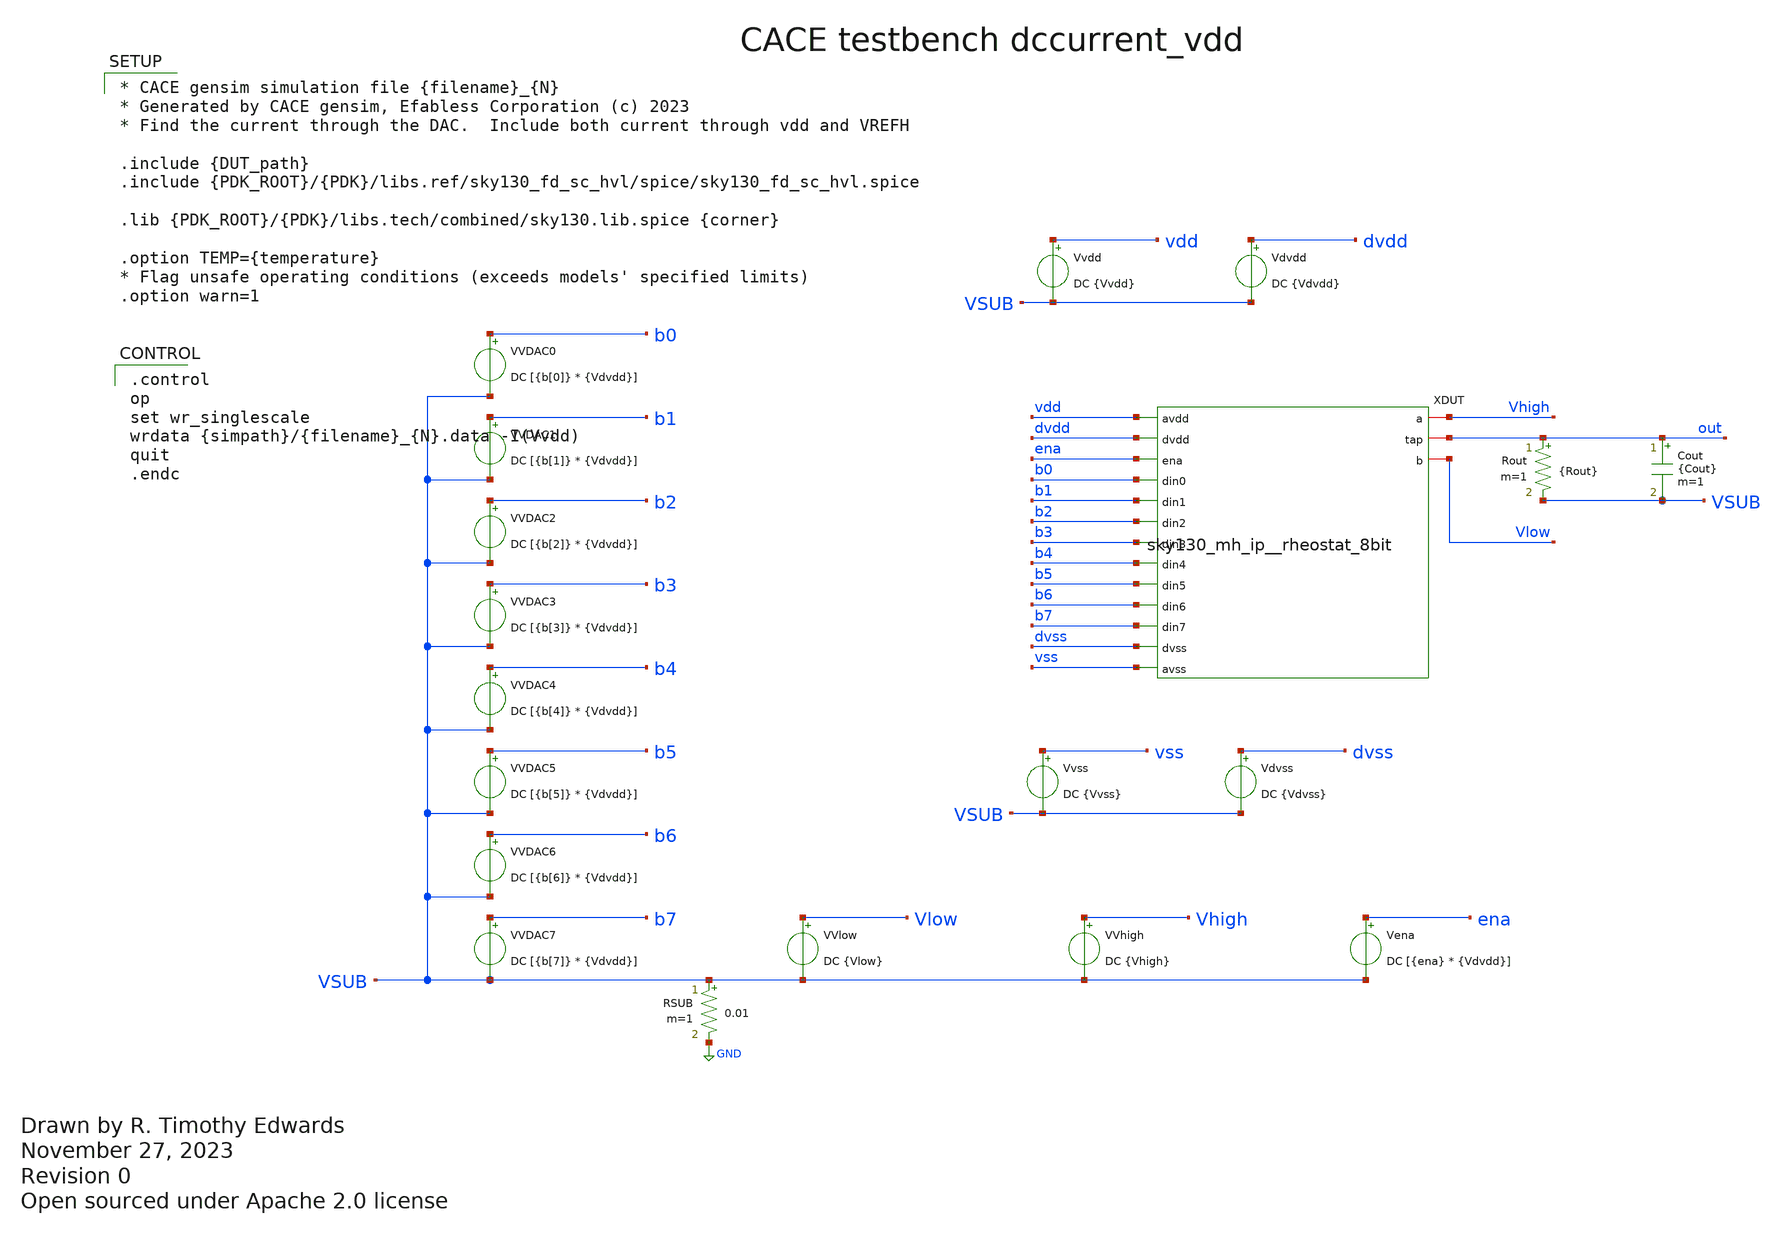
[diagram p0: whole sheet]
** sch_path: cace/dccurrent_vdd.sch
* Open sourced under Apache 2.0 license
**.subckt dccurrent_vdd
VVDAC7 b7 VSUB DC [{b[7]} * {Vdvdd}]
VVDAC1 b1 VSUB DC [{b[1]} * {Vdvdd}]
VVDAC2 b2 VSUB DC [{b[2]} * {Vdvdd}]
VVDAC3 b3 VSUB DC [{b[3]} * {Vdvdd}]
VVDAC4 b4 VSUB DC [{b[4]} * {Vdvdd}]
VVDAC5 b5 VSUB DC [{b[5]} * {Vdvdd}]
VVDAC6 b6 VSUB DC [{b[6]} * {Vdvdd}]
VVDAC0 b0 VSUB DC [{b[0]} * {Vdvdd}]
VVlow Vlow VSUB DC {Vlow}
VVhigh Vhigh VSUB DC {Vhigh}
Vena ena VSUB DC [{ena} * {Vdvdd}]
Vvss vss VSUB DC {Vvss}
Rout out VSUB {Rout} m=1
Cout out VSUB {Cout} m=1
Vdvss dvss VSUB DC {Vdvss}
Vvdd vdd VSUB DC {Vvdd}
Vdvdd dvdd VSUB DC {Vdvdd}
RSUB VSUB GND 0.01 m=1
XDUT vdd dvdd ena b0 Vhigh b1 b2 out b3 Vlow b4 b5 b6 b7 dvss vss sky130_mh_ip__rheostat_8bit
**** begin user architecture code

.control
op
set wr_singlescale
wrdata {simpath}/{filename}_{N}.data -I(Vvdd)
quit
.endc



* CACE gensim simulation file {filename}_{N}
* Generated by CACE gensim, Efabless Corporation (c) 2023
* Find the current through the DAC.  Include both current through vdd and VREFH

.include {DUT_path}
.include {PDK_ROOT}/{PDK}/libs.ref/sky130_fd_sc_hvl/spice/sky130_fd_sc_hvl.spice

.lib {PDK_ROOT}/{PDK}/libs.tech/combined/sky130.lib.spice {corner}

.option TEMP={temperature}
* Flag unsafe operating conditions (exceeds models' specified limits)
.option warn=1


**** end user architecture code
**.ends

* expanding   symbol:  sky130_mh_ip__rheostat_8bit.sym # of pins=16
** sym_path: xschem/sky130_mh_ip__rheostat_8bit.sym
** sch_path: xschem/sky130_mh_ip__rheostat_8bit.sch
.subckt sky130_mh_ip__rheostat_8bit avdd dvdd ena din0 a din1 din2 tap din3 b din4 din5 din6 din7 dvss avss
*.ipin din0
*.ipin din1
*.ipin din2
*.ipin din3
*.ipin din4
*.ipin din5
*.ipin din6
*.ipin din7
*.iopin a
*.iopin tap
*.iopin b
*.ipin dvss
*.ipin avdd
*.ipin avss
*.ipin ena
*.ipin dvdd
x1 avdd nb0 nb5 nb6 nb3 nb4 nb1 nb7 nb2 a tap pb3 pb2 pb4 pb1 pb5 pb7 pb6 pb0 avss 8bit_half_rheostat
x2 avdd dvdd nb0 ena pb0 din0 dvss avss double_output_buffer
x3 avdd dvdd nb1 ena pb1 din1 dvss avss double_output_buffer
x4 avdd dvdd nb2 ena pb2 din2 dvss avss double_output_buffer
x5 avdd dvdd nb3 ena pb3 din3 dvss avss double_output_buffer
x6 avdd dvdd nb4 ena pb4 din4 dvss avss double_output_buffer
x7 avdd dvdd nb5 ena pb5 din5 dvss avss double_output_buffer
x8 avdd dvdd nb6 ena pb6 din6 dvss avss double_output_buffer
x9 avdd dvdd nb7 ena pb7 din7 dvss avss double_output_buffer
x10 avdd pb0 pb5 pb6 pb3 pb4 pb1 pb7 pb2 tap b nb3 nb2 nb4 nb1 nb5 nb7 nb6 nb0 avss 8bit_half_rheostat
.ends


* expanding   symbol:  8bit_half_rheostat.sym # of pins=20
** sym_path: xschem/8bit_half_rheostat.sym
** sch_path: xschem/8bit_half_rheostat.sch
.subckt 8bit_half_rheostat avdd inn0 inn5 inn6 inn3 inn4 inn1 inn7 inn2 a b inp3 inp2 inp4 inp1 inp5 inp7 inp6 inp0 avss
*.iopin b
*.iopin a
*.ipin inn0
*.ipin inn1
*.ipin inn2
*.ipin inn3
*.ipin inn4
*.ipin inn5
*.ipin inn6
*.ipin inn7
*.ipin inp0
*.ipin inp1
*.ipin inp2
*.ipin inp3
*.ipin inp4
*.ipin inp5
*.ipin inp6
*.ipin inp7
*.ipin avdd
*.ipin avss
XM17 a inn0 net1 avdd sky130_fd_pr__pfet_g5v0d10v5 L=0.5 W=10 nf=1 ad='int((nf+1)/2) * W/nf * 0.29' as='int((nf+2)/2)
+ * W/nf * 0.29' pd='2*int((nf+1)/2) * (W/nf + 0.29)' ps='2*int((nf+2)/2) * (W/nf + 0.29)' nrd='0.29 /
+ W' nrs='0.29 / W' sa=0 sb=0 sd=0 mult=1 m=1
XM18 a inp0 net1 avss sky130_fd_pr__nfet_g5v0d10v5 L=0.5 W=10 nf=1 ad='int((nf+1)/2) * W/nf * 0.29' as='int((nf+2)/2)
+ * W/nf * 0.29' pd='2*int((nf+1)/2) * (W/nf + 0.29)' ps='2*int((nf+2)/2) * (W/nf + 0.29)' nrd='0.29 /
+ W' nrs='0.29 / W' sa=0 sb=0 sd=0 mult=1 m=1
XM19 net1 inn1 net2 avdd sky130_fd_pr__pfet_g5v0d10v5 L=0.5 W=10 nf=1 ad='int((nf+1)/2) * W/nf * 0.29' as='int((nf+2)/2)
+ * W/nf * 0.29' pd='2*int((nf+1)/2) * (W/nf + 0.29)' ps='2*int((nf+2)/2) * (W/nf + 0.29)' nrd='0.29 /
+ W' nrs='0.29 / W' sa=0 sb=0 sd=0 mult=1 m=1
XM20 net1 inp1 net2 avss sky130_fd_pr__nfet_g5v0d10v5 L=0.5 W=10 nf=1 ad='int((nf+1)/2) * W/nf * 0.29' as='int((nf+2)/2)
+ * W/nf * 0.29' pd='2*int((nf+1)/2) * (W/nf + 0.29)' ps='2*int((nf+2)/2) * (W/nf + 0.29)' nrd='0.29 /
+ W' nrs='0.29 / W' sa=0 sb=0 sd=0 mult=1 m=1
XM21 net2 inn2 net3 avdd sky130_fd_pr__pfet_g5v0d10v5 L=0.5 W=10 nf=1 ad='int((nf+1)/2) * W/nf * 0.29' as='int((nf+2)/2)
+ * W/nf * 0.29' pd='2*int((nf+1)/2) * (W/nf + 0.29)' ps='2*int((nf+2)/2) * (W/nf + 0.29)' nrd='0.29 /
+ W' nrs='0.29 / W' sa=0 sb=0 sd=0 mult=1 m=1
XM22 net2 inp2 net3 avss sky130_fd_pr__nfet_g5v0d10v5 L=0.5 W=10 nf=1 ad='int((nf+1)/2) * W/nf * 0.29' as='int((nf+2)/2)
+ * W/nf * 0.29' pd='2*int((nf+1)/2) * (W/nf + 0.29)' ps='2*int((nf+2)/2) * (W/nf + 0.29)' nrd='0.29 /
+ W' nrs='0.29 / W' sa=0 sb=0 sd=0 mult=1 m=1
XM23 net3 inn3 net4 avdd sky130_fd_pr__pfet_g5v0d10v5 L=0.5 W=10 nf=1 ad='int((nf+1)/2) * W/nf * 0.29' as='int((nf+2)/2)
+ * W/nf * 0.29' pd='2*int((nf+1)/2) * (W/nf + 0.29)' ps='2*int((nf+2)/2) * (W/nf + 0.29)' nrd='0.29 /
+ W' nrs='0.29 / W' sa=0 sb=0 sd=0 mult=1 m=1
XM24 net3 inp3 net4 avss sky130_fd_pr__nfet_g5v0d10v5 L=0.5 W=10 nf=1 ad='int((nf+1)/2) * W/nf * 0.29' as='int((nf+2)/2)
+ * W/nf * 0.29' pd='2*int((nf+1)/2) * (W/nf + 0.29)' ps='2*int((nf+2)/2) * (W/nf + 0.29)' nrd='0.29 /
+ W' nrs='0.29 / W' sa=0 sb=0 sd=0 mult=1 m=1
XM25 net4 inn4 net5 avdd sky130_fd_pr__pfet_g5v0d10v5 L=0.5 W=10 nf=1 ad='int((nf+1)/2) * W/nf * 0.29' as='int((nf+2)/2)
+ * W/nf * 0.29' pd='2*int((nf+1)/2) * (W/nf + 0.29)' ps='2*int((nf+2)/2) * (W/nf + 0.29)' nrd='0.29 /
+ W' nrs='0.29 / W' sa=0 sb=0 sd=0 mult=1 m=1
XM26 net4 inp4 net5 avss sky130_fd_pr__nfet_g5v0d10v5 L=0.5 W=10 nf=1 ad='int((nf+1)/2) * W/nf * 0.29' as='int((nf+2)/2)
+ * W/nf * 0.29' pd='2*int((nf+1)/2) * (W/nf + 0.29)' ps='2*int((nf+2)/2) * (W/nf + 0.29)' nrd='0.29 /
+ W' nrs='0.29 / W' sa=0 sb=0 sd=0 mult=1 m=1
XM27 net5 inn5 net6 avdd sky130_fd_pr__pfet_g5v0d10v5 L=0.5 W=10 nf=1 ad='int((nf+1)/2) * W/nf * 0.29' as='int((nf+2)/2)
+ * W/nf * 0.29' pd='2*int((nf+1)/2) * (W/nf + 0.29)' ps='2*int((nf+2)/2) * (W/nf + 0.29)' nrd='0.29 /
+ W' nrs='0.29 / W' sa=0 sb=0 sd=0 mult=1 m=1
XM28 net5 inp5 net6 avss sky130_fd_pr__nfet_g5v0d10v5 L=0.5 W=10 nf=1 ad='int((nf+1)/2) * W/nf * 0.29' as='int((nf+2)/2)
+ * W/nf * 0.29' pd='2*int((nf+1)/2) * (W/nf + 0.29)' ps='2*int((nf+2)/2) * (W/nf + 0.29)' nrd='0.29 /
+ W' nrs='0.29 / W' sa=0 sb=0 sd=0 mult=1 m=1
XM29 net6 inn6 net7 avdd sky130_fd_pr__pfet_g5v0d10v5 L=0.5 W=10 nf=1 ad='int((nf+1)/2) * W/nf * 0.29' as='int((nf+2)/2)
+ * W/nf * 0.29' pd='2*int((nf+1)/2) * (W/nf + 0.29)' ps='2*int((nf+2)/2) * (W/nf + 0.29)' nrd='0.29 /
+ W' nrs='0.29 / W' sa=0 sb=0 sd=0 mult=1 m=1
XM30 net6 inp6 net7 avss sky130_fd_pr__nfet_g5v0d10v5 L=0.5 W=10 nf=1 ad='int((nf+1)/2) * W/nf * 0.29' as='int((nf+2)/2)
+ * W/nf * 0.29' pd='2*int((nf+1)/2) * (W/nf + 0.29)' ps='2*int((nf+2)/2) * (W/nf + 0.29)' nrd='0.29 /
+ W' nrs='0.29 / W' sa=0 sb=0 sd=0 mult=1 m=1
XM31 net7 inn7 b avdd sky130_fd_pr__pfet_g5v0d10v5 L=0.5 W=10 nf=1 ad='int((nf+1)/2) * W/nf * 0.29' as='int((nf+2)/2)
+ * W/nf * 0.29' pd='2*int((nf+1)/2) * (W/nf + 0.29)' ps='2*int((nf+2)/2) * (W/nf + 0.29)' nrd='0.29 /
+ W' nrs='0.29 / W' sa=0 sb=0 sd=0 mult=1 m=1
XM32 net7 inp7 b avss sky130_fd_pr__nfet_g5v0d10v5 L=0.5 W=10 nf=1 ad='int((nf+1)/2) * W/nf * 0.29' as='int((nf+2)/2)
+ * W/nf * 0.29' pd='2*int((nf+1)/2) * (W/nf + 0.29)' ps='2*int((nf+2)/2) * (W/nf + 0.29)' nrd='0.29 /
+ W' nrs='0.29 / W' sa=0 sb=0 sd=0 mult=1 m=1
XR9 a net1 sky130_fd_pr__res_generic_po W=0.957 L=2 m=1
XR10 net1 net2 sky130_fd_pr__res_generic_po W=0.957 L=4 m=1
XR11 net2 net3 sky130_fd_pr__res_generic_po W=0.957 L=8 m=1
XR12 net3 net4 sky130_fd_pr__res_generic_po W=0.957 L=16 m=1
XR13 net4 net5 sky130_fd_pr__res_generic_po W=0.957 L=32 m=1
XR14 net5 net6 sky130_fd_pr__res_generic_po W=0.957 L=64 m=1
XR15 net6 net7 sky130_fd_pr__res_generic_po W=0.957 L=128 m=1
XR16 net7 b sky130_fd_pr__res_generic_po W=0.957 L=256 m=1
.ends


* expanding   symbol:  double_output_buffer.sym # of pins=8
** sym_path: xschem/double_output_buffer.sym
** sch_path: xschem/double_output_buffer.sch
.subckt double_output_buffer avdd dvdd nout en pout din dvss avss
*.ipin din
*.ipin dvdd
*.ipin dvss
*.opin pout
*.opin nout
*.ipin en
*.ipin avdd
*.ipin avss
XM1 net1 en dvdd dvdd sky130_fd_pr__pfet_01v8 L=0.15 W=1 nf=1 ad='int((nf+1)/2) * W/nf * 0.29' as='int((nf+2)/2)
+ * W/nf * 0.29' pd='2*int((nf+1)/2) * (W/nf + 0.29)' ps='2*int((nf+2)/2) * (W/nf + 0.29)' nrd='0.29 /
+ W' nrs='0.29 / W' sa=0 sb=0 sd=0 mult=1 m=1
XM2 net1 din dvdd dvdd sky130_fd_pr__pfet_01v8 L=0.15 W=1 nf=1 ad='int((nf+1)/2) * W/nf * 0.29' as='int((nf+2)/2)
+ * W/nf * 0.29' pd='2*int((nf+1)/2) * (W/nf + 0.29)' ps='2*int((nf+2)/2) * (W/nf + 0.29)' nrd='0.29 /
+ W' nrs='0.29 / W' sa=0 sb=0 sd=0 mult=1 m=1
XM3 net3 net1 dvdd dvdd sky130_fd_pr__pfet_01v8 L=0.15 W=1 nf=1 ad='int((nf+1)/2) * W/nf * 0.29' as='int((nf+2)/2)
+ * W/nf * 0.29' pd='2*int((nf+1)/2) * (W/nf + 0.29)' ps='2*int((nf+2)/2) * (W/nf + 0.29)' nrd='0.29 /
+ W' nrs='0.29 / W' sa=0 sb=0 sd=0 mult=1 m=1
XM4 net1 en net2 dvss sky130_fd_pr__nfet_01v8 L=0.15 W=1 nf=1 ad='int((nf+1)/2) * W/nf * 0.29' as='int((nf+2)/2)
+ * W/nf * 0.29' pd='2*int((nf+1)/2) * (W/nf + 0.29)' ps='2*int((nf+2)/2) * (W/nf + 0.29)' nrd='0.29 /
+ W' nrs='0.29 / W' sa=0 sb=0 sd=0 mult=1 m=1
XM5 net2 din dvss dvss sky130_fd_pr__nfet_01v8 L=0.15 W=1 nf=1 ad='int((nf+1)/2) * W/nf * 0.29' as='int((nf+2)/2)
+ * W/nf * 0.29' pd='2*int((nf+1)/2) * (W/nf + 0.29)' ps='2*int((nf+2)/2) * (W/nf + 0.29)' nrd='0.29 /
+ W' nrs='0.29 / W' sa=0 sb=0 sd=0 mult=1 m=1
XM6 net3 net1 dvss dvss sky130_fd_pr__nfet_01v8 L=0.15 W=1 nf=1 ad='int((nf+1)/2) * W/nf * 0.29' as='int((nf+2)/2)
+ * W/nf * 0.29' pd='2*int((nf+1)/2) * (W/nf + 0.29)' ps='2*int((nf+2)/2) * (W/nf + 0.29)' nrd='0.29 /
+ W' nrs='0.29 / W' sa=0 sb=0 sd=0 mult=1 m=1
XM7 nout net3 avdd avdd sky130_fd_pr__pfet_g5v0d10v5 L=1 W=2 nf=1 ad='int((nf+1)/2) * W/nf * 0.29' as='int((nf+2)/2)
+ * W/nf * 0.29' pd='2*int((nf+1)/2) * (W/nf + 0.29)' ps='2*int((nf+2)/2) * (W/nf + 0.29)' nrd='0.29 /
+ W' nrs='0.29 / W' sa=0 sb=0 sd=0 mult=1 m=1
XM8 nout net3 avss avss sky130_fd_pr__nfet_g5v0d10v5 L=1 W=2 nf=1 ad='int((nf+1)/2) * W/nf * 0.29' as='int((nf+2)/2)
+ * W/nf * 0.29' pd='2*int((nf+1)/2) * (W/nf + 0.29)' ps='2*int((nf+2)/2) * (W/nf + 0.29)' nrd='0.29 /
+ W' nrs='0.29 / W' sa=0 sb=0 sd=0 mult=1 m=1
XM9 pout nout avdd avdd sky130_fd_pr__pfet_g5v0d10v5 L=1 W=2 nf=1 ad='int((nf+1)/2) * W/nf * 0.29' as='int((nf+2)/2)
+ * W/nf * 0.29' pd='2*int((nf+1)/2) * (W/nf + 0.29)' ps='2*int((nf+2)/2) * (W/nf + 0.29)' nrd='0.29 /
+ W' nrs='0.29 / W' sa=0 sb=0 sd=0 mult=1 m=1
XM10 pout nout net4 net4 sky130_fd_pr__nfet_g5v0d10v5 L=1 W=2 nf=1 ad='int((nf+1)/2) * W/nf * 0.29' as='int((nf+2)/2)
+ * W/nf * 0.29' pd='2*int((nf+1)/2) * (W/nf + 0.29)' ps='2*int((nf+2)/2) * (W/nf + 0.29)' nrd='0.29 /
+ W' nrs='0.29 / W' sa=0 sb=0 sd=0 mult=1 m=1
.ends

.GLOBAL GND
.end
